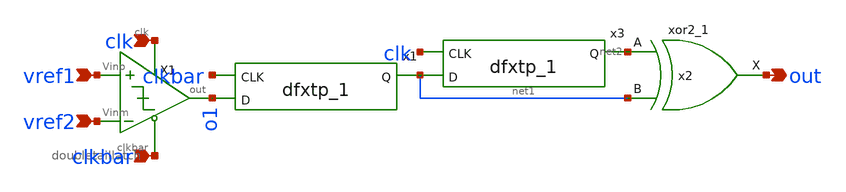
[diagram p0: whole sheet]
** sch_path: xschem/comparator/dlatch_comp_LVS.sch
**.subckt dlatch_comp_LVS vref1 out clk clkbar vref2
*.ipin vref1
*.opin out
*.ipin clk
*.ipin clkbar
*.ipin vref2
X1 vref1 vref2 o1 clk clkbar doubletaillatch
x2 net2 net1 GND GND VDD VDD out sky130_fd_sc_lp__xor2_1
x1 clkbar o1 GND GND VDD VDD net1 sky130_fd_sc_lp__dfxtp_1
x3 clk net1 GND GND VDD VDD net2 sky130_fd_sc_lp__dfxtp_1
**.ends

* expanding   symbol:  /home/sky/fossi_cochlea/xschem/comparator/doubletaillatch.sym # of pins=5
** sym_path: xschem/comparator/doubletaillatch.sym
** sch_path: xschem/comparator/doubletaillatch.sch
.subckt doubletaillatch Vinp Vinm out clk clkbar
*.ipin clkbar
*.opin out
*.ipin Vinp
*.ipin Vinm
*.ipin clk
XM3 net6 out VDD VDD sky130_fd_pr__pfet_01v8 L=1 W=4 nf=1 ad='int((nf+1)/2) * W/nf * 0.29' as='int((nf+2)/2) * W/nf * 0.29'
+ pd='2*int((nf+1)/2) * (W/nf + 0.29)' ps='2*int((nf+2)/2) * (W/nf + 0.29)' nrd='0.29 / W' nrs='0.29 / W'
+ sa=0 sb=0 sd=0 mult=1 m=1
XM4 VDD net1 net7 VDD sky130_fd_pr__pfet_01v8 L=1 W=4 nf=1 ad='int((nf+1)/2) * W/nf * 0.29' as='int((nf+2)/2) * W/nf * 0.29'
+ pd='2*int((nf+1)/2) * (W/nf + 0.29)' ps='2*int((nf+2)/2) * (W/nf + 0.29)' nrd='0.29 / W' nrs='0.29 / W'
+ sa=0 sb=0 sd=0 mult=1 m=1
XM5 net7 net3 out VDD sky130_fd_pr__pfet_01v8 L=1 W=4 nf=1 ad='int((nf+1)/2) * W/nf * 0.29' as='int((nf+2)/2) * W/nf * 0.29'
+ pd='2*int((nf+1)/2) * (W/nf + 0.29)' ps='2*int((nf+2)/2) * (W/nf + 0.29)' nrd='0.29 / W' nrs='0.29 / W'
+ sa=0 sb=0 sd=0 mult=1 m=1
XM6 net1 net4 net6 VDD sky130_fd_pr__pfet_01v8 L=1 W=4 nf=1 ad='int((nf+1)/2) * W/nf * 0.29' as='int((nf+2)/2) * W/nf * 0.29'
+ pd='2*int((nf+1)/2) * (W/nf + 0.29)' ps='2*int((nf+2)/2) * (W/nf + 0.29)' nrd='0.29 / W' nrs='0.29 / W'
+ sa=0 sb=0 sd=0 mult=1 m=1
XM7 out clkbar GND GND sky130_fd_pr__nfet_01v8 L=1 W=2 nf=1 ad='int((nf+1)/2) * W/nf * 0.29' as='int((nf+2)/2) * W/nf * 0.29'
+ pd='2*int((nf+1)/2) * (W/nf + 0.29)' ps='2*int((nf+2)/2) * (W/nf + 0.29)' nrd='0.29 / W' nrs='0.29 / W'
+ sa=0 sb=0 sd=0 mult=1 m=1
XM8 GND net1 out GND sky130_fd_pr__nfet_01v8 L=1 W=2 nf=1 ad='int((nf+1)/2) * W/nf * 0.29' as='int((nf+2)/2) * W/nf * 0.29'
+ pd='2*int((nf+1)/2) * (W/nf + 0.29)' ps='2*int((nf+2)/2) * (W/nf + 0.29)' nrd='0.29 / W' nrs='0.29 / W'
+ sa=0 sb=0 sd=0 mult=1 m=1
XM9 net1 out GND GND sky130_fd_pr__nfet_01v8 L=1 W=2 nf=1 ad='int((nf+1)/2) * W/nf * 0.29' as='int((nf+2)/2) * W/nf * 0.29'
+ pd='2*int((nf+1)/2) * (W/nf + 0.29)' ps='2*int((nf+2)/2) * (W/nf + 0.29)' nrd='0.29 / W' nrs='0.29 / W'
+ sa=0 sb=0 sd=0 mult=1 m=1
XM10 GND clkbar net1 GND sky130_fd_pr__nfet_01v8 L=1 W=2 nf=1 ad='int((nf+1)/2) * W/nf * 0.29' as='int((nf+2)/2) * W/nf * 0.29'
+ pd='2*int((nf+1)/2) * (W/nf + 0.29)' ps='2*int((nf+2)/2) * (W/nf + 0.29)' nrd='0.29 / W' nrs='0.29 / W'
+ sa=0 sb=0 sd=0 mult=1 m=1
XM11 net4 clk VDD VDD sky130_fd_pr__pfet_01v8 L=1 W=4 nf=1 ad='int((nf+1)/2) * W/nf * 0.29' as='int((nf+2)/2) * W/nf * 0.29'
+ pd='2*int((nf+1)/2) * (W/nf + 0.29)' ps='2*int((nf+2)/2) * (W/nf + 0.29)' nrd='0.29 / W' nrs='0.29 / W'
+ sa=0 sb=0 sd=0 mult=1 m=1
XM12 VDD clk net3 VDD sky130_fd_pr__pfet_01v8 L=1 W=4 nf=1 ad='int((nf+1)/2) * W/nf * 0.29' as='int((nf+2)/2) * W/nf * 0.29'
+ pd='2*int((nf+1)/2) * (W/nf + 0.29)' ps='2*int((nf+2)/2) * (W/nf + 0.29)' nrd='0.29 / W' nrs='0.29 / W'
+ sa=0 sb=0 sd=0 mult=1 m=1
XM13 net4 Vinm net2 GND sky130_fd_pr__nfet_01v8 L=1 W=2 nf=1 ad='int((nf+1)/2) * W/nf * 0.29' as='int((nf+2)/2) * W/nf * 0.29'
+ pd='2*int((nf+1)/2) * (W/nf + 0.29)' ps='2*int((nf+2)/2) * (W/nf + 0.29)' nrd='0.29 / W' nrs='0.29 / W'
+ sa=0 sb=0 sd=0 mult=1 m=1
XM14 net2 Vinp net3 GND sky130_fd_pr__nfet_01v8 L=1 W=2 nf=1 ad='int((nf+1)/2) * W/nf * 0.29' as='int((nf+2)/2) * W/nf * 0.29'
+ pd='2*int((nf+1)/2) * (W/nf + 0.29)' ps='2*int((nf+2)/2) * (W/nf + 0.29)' nrd='0.29 / W' nrs='0.29 / W'
+ sa=0 sb=0 sd=0 mult=1 m=1
XM15 net2 clk net5 GND sky130_fd_pr__nfet_01v8 L=1 W=2 nf=1 ad='int((nf+1)/2) * W/nf * 0.29' as='int((nf+2)/2) * W/nf * 0.29'
+ pd='2*int((nf+1)/2) * (W/nf + 0.29)' ps='2*int((nf+2)/2) * (W/nf + 0.29)' nrd='0.29 / W' nrs='0.29 / W'
+ sa=0 sb=0 sd=0 mult=1 m=1
XM16 net5 clkbar GND GND sky130_fd_pr__nfet_01v8 L=1 W=2 nf=1 ad='int((nf+1)/2) * W/nf * 0.29' as='int((nf+2)/2) * W/nf * 0.29'
+ pd='2*int((nf+1)/2) * (W/nf + 0.29)' ps='2*int((nf+2)/2) * (W/nf + 0.29)' nrd='0.29 / W' nrs='0.29 / W'
+ sa=0 sb=0 sd=0 mult=1 m=1
XC2 net5 GND sky130_fd_pr__cap_mim_m3_1 W=10 L=10 MF=1 m=1
XC1 net4 GND sky130_fd_pr__cap_mim_m3_1 W=1 L=1 MF=1 m=1
XC3 net3 GND sky130_fd_pr__cap_mim_m3_1 W=1 L=1 MF=1 m=1
.ends

.GLOBAL VDD
.GLOBAL GND
.end
